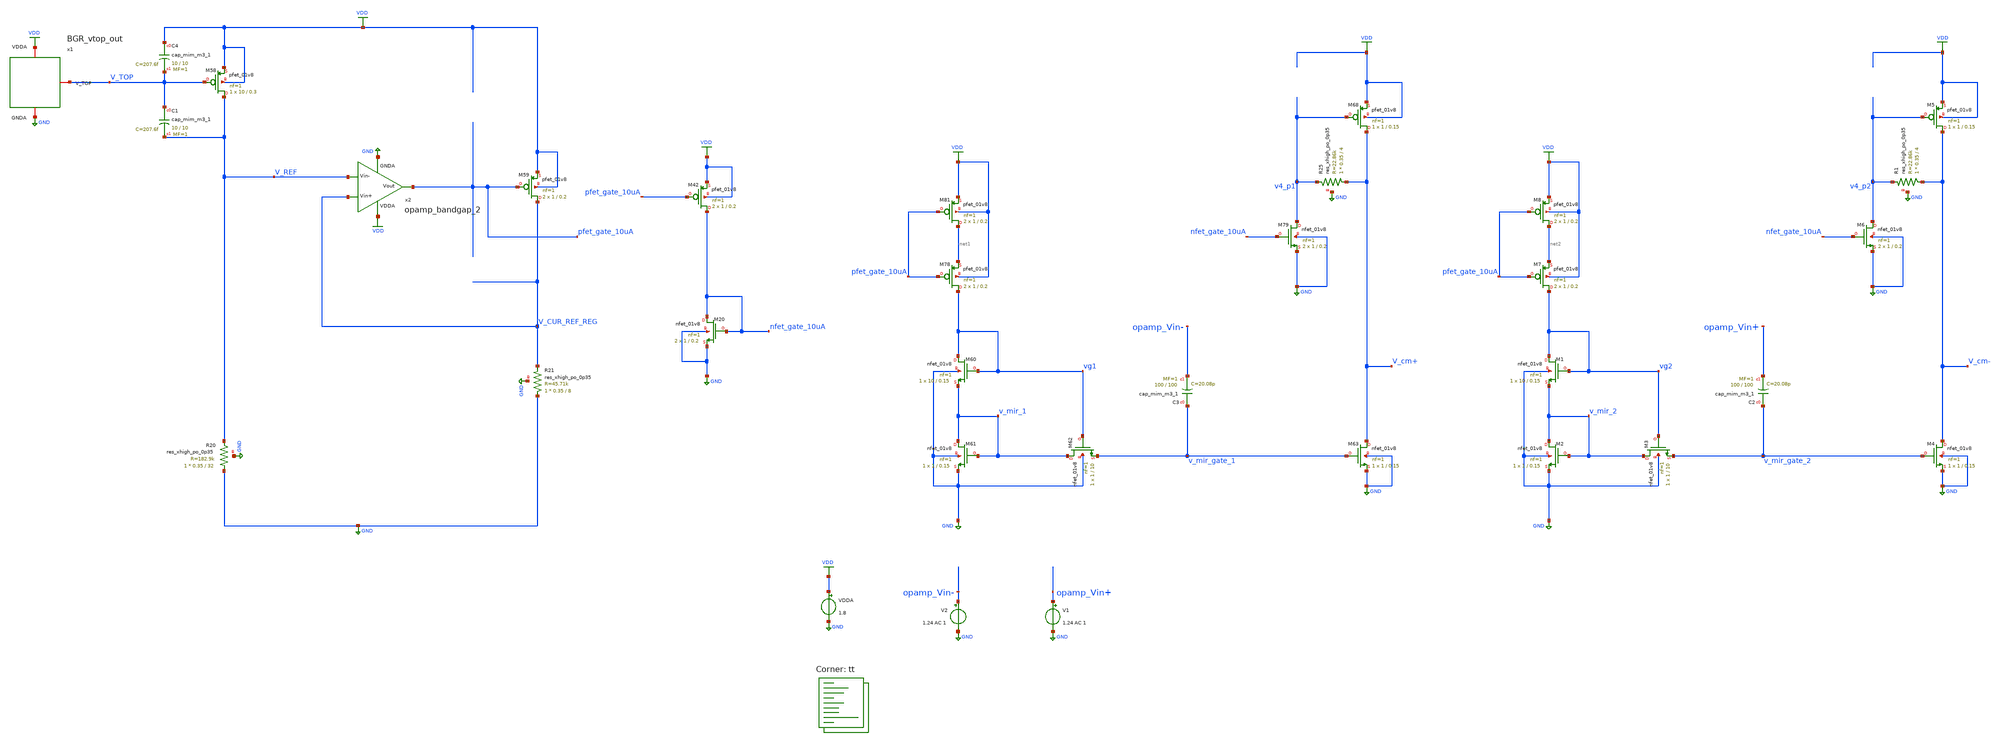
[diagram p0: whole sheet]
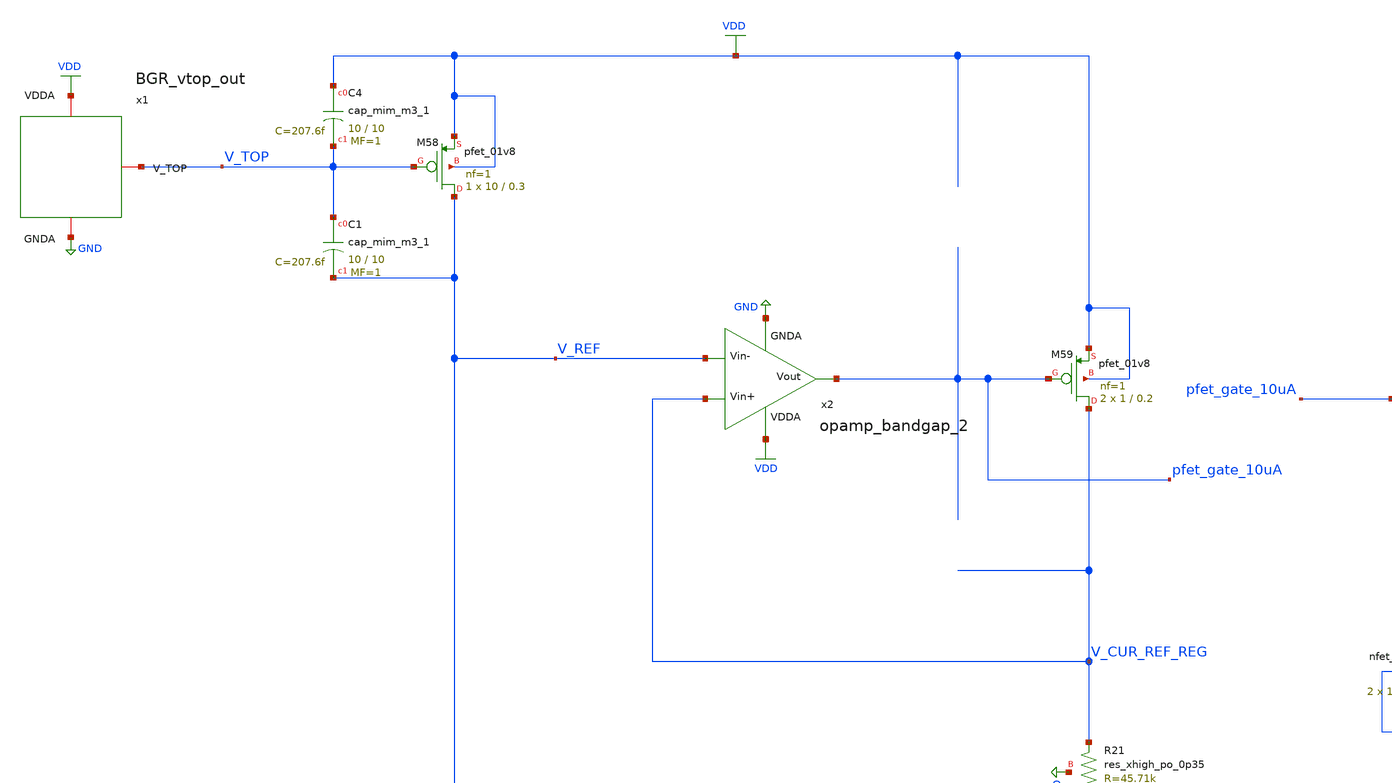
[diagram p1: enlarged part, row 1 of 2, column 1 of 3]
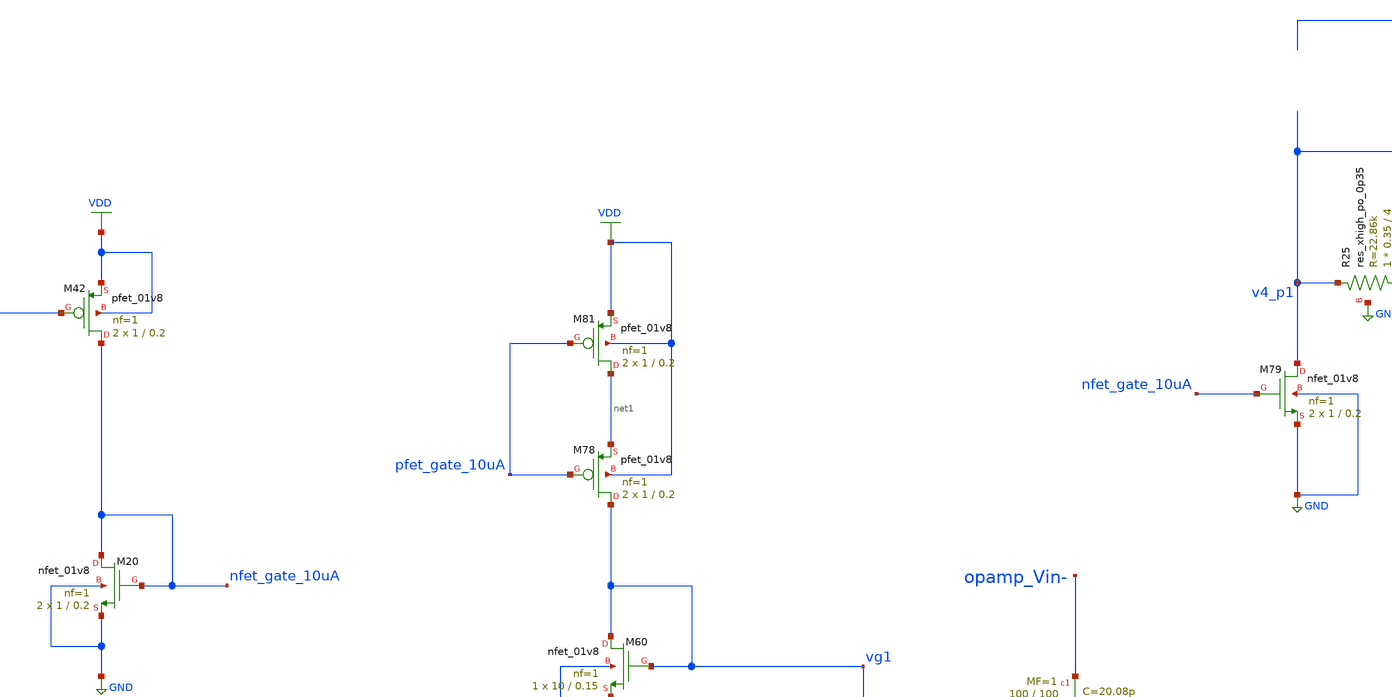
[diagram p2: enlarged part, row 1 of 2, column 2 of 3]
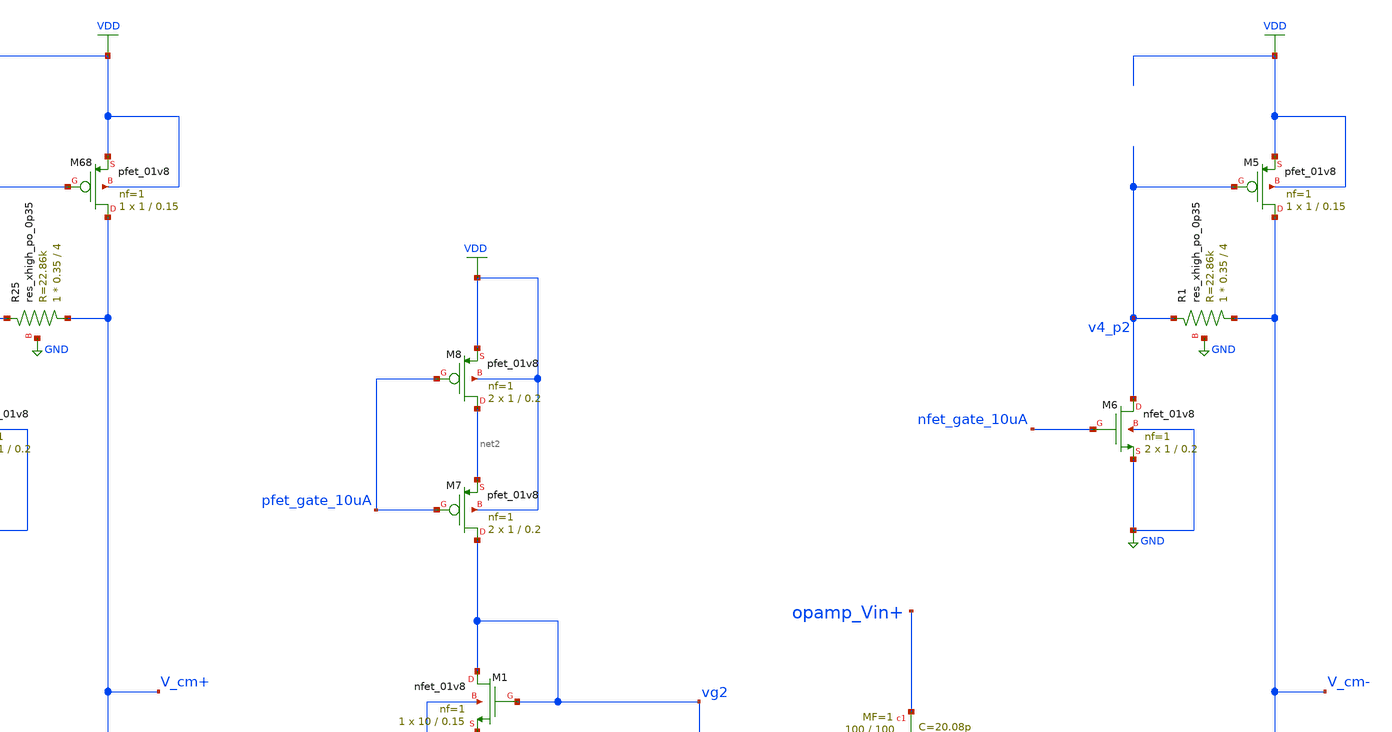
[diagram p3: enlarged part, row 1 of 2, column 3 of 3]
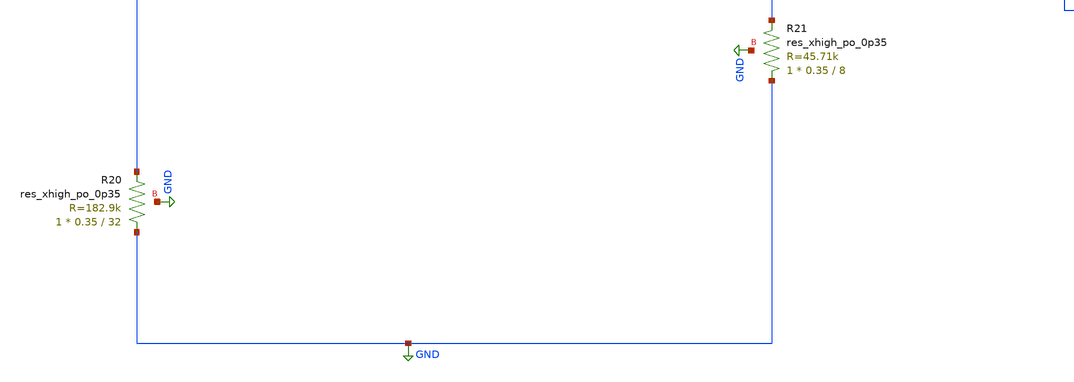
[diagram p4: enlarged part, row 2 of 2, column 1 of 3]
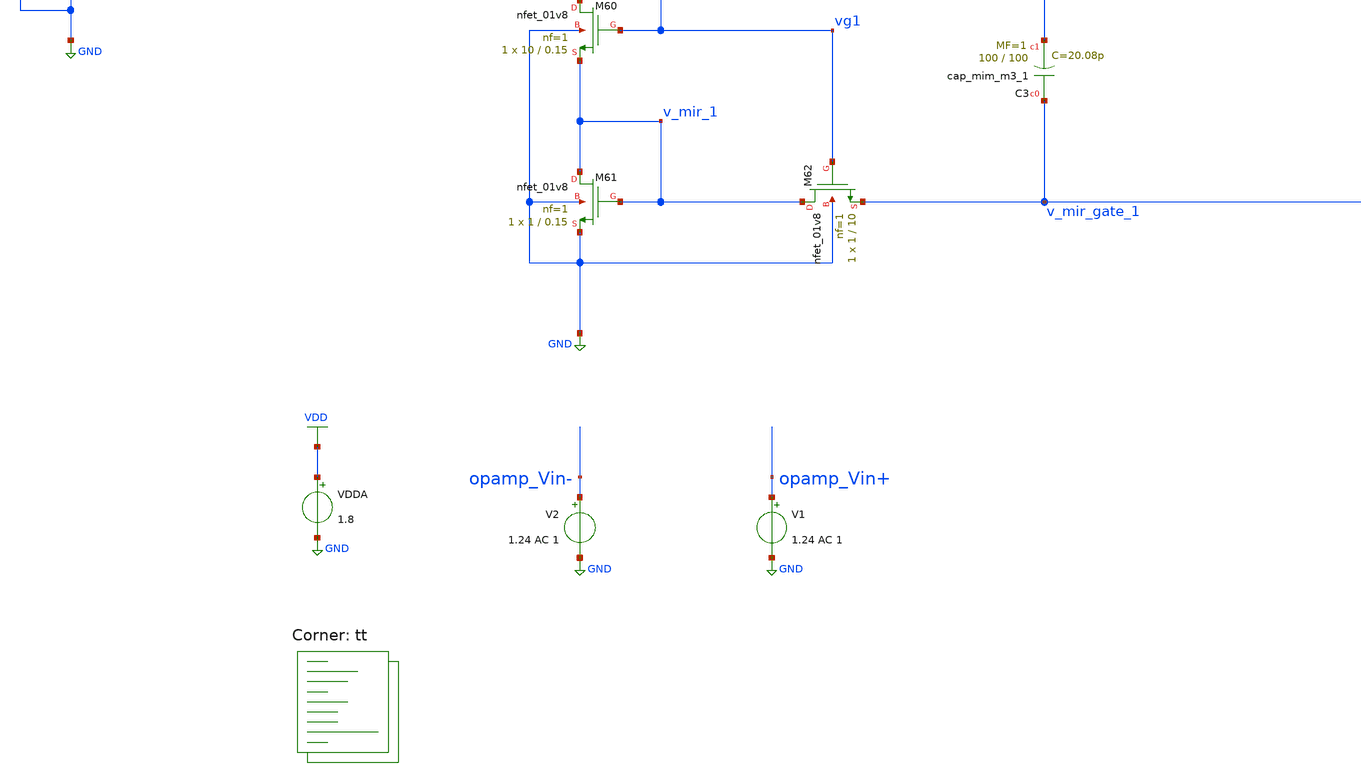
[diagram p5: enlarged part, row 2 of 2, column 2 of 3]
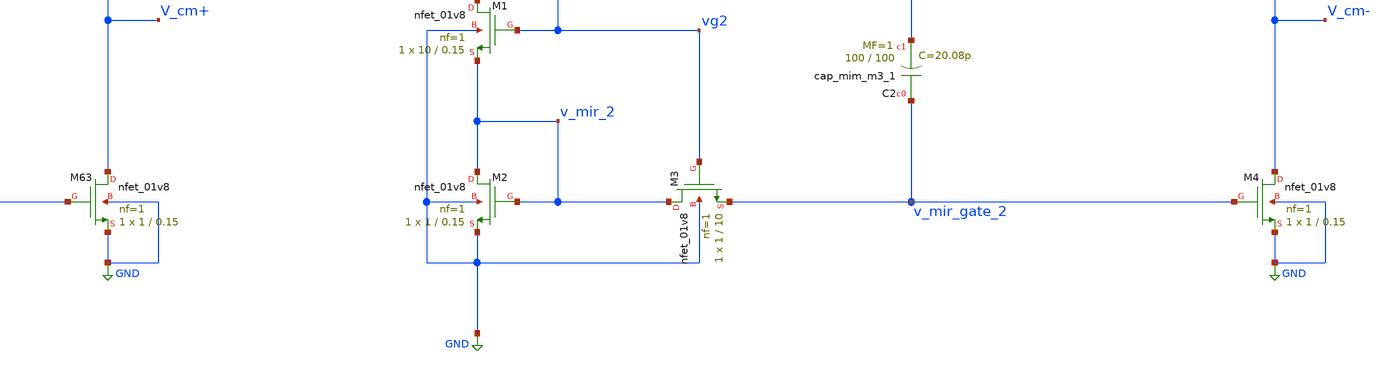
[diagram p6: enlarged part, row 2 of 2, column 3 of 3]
** sch_path: projects/opamp/xschem_ngspice/tb_input_stage.sch
**.subckt tb_input_stage
VDDA VDD GND 1.8
XC3 v_mir_gate_1 opamp_Vin- sky130_fd_pr__cap_mim_m3_1 W=100 L=100 MF=1 m=1
XM60 vg1 vg1 v_mir_1 GND sky130_fd_pr__nfet_01v8 L=0.15 W=10 nf=1 ad='int((nf+1)/2) * W/nf * 0.29' as='int((nf+2)/2) * W/nf * 0.29'
+ pd='2*int((nf+1)/2) * (W/nf + 0.29)' ps='2*int((nf+2)/2) * (W/nf + 0.29)' nrd='0.29 / W' nrs='0.29 / W'
+ sa=0 sb=0 sd=0 mult=1 m=1
XM61 v_mir_1 v_mir_1 GND GND sky130_fd_pr__nfet_01v8 L=0.15 W=1 nf=1 ad='int((nf+1)/2) * W/nf * 0.29'
+ as='int((nf+2)/2) * W/nf * 0.29' pd='2*int((nf+1)/2) * (W/nf + 0.29)' ps='2*int((nf+2)/2) * (W/nf + 0.29)'
+ nrd='0.29 / W' nrs='0.29 / W' sa=0 sb=0 sd=0 mult=1 m=1
XM62 v_mir_1 vg1 v_mir_gate_1 GND sky130_fd_pr__nfet_01v8 L=10 W=1 nf=1 ad='int((nf+1)/2) * W/nf * 0.29'
+ as='int((nf+2)/2) * W/nf * 0.29' pd='2*int((nf+1)/2) * (W/nf + 0.29)' ps='2*int((nf+2)/2) * (W/nf + 0.29)'
+ nrd='0.29 / W' nrs='0.29 / W' sa=0 sb=0 sd=0 mult=1 m=1
XM63 V_cm+ v_mir_gate_1 GND GND sky130_fd_pr__nfet_01v8 L=0.15 W=1 nf=1 ad='int((nf+1)/2) * W/nf * 0.29'
+ as='int((nf+2)/2) * W/nf * 0.29' pd='2*int((nf+1)/2) * (W/nf + 0.29)' ps='2*int((nf+2)/2) * (W/nf + 0.29)'
+ nrd='0.29 / W' nrs='0.29 / W' sa=0 sb=0 sd=0 mult=1 m=1
XM68 V_cm+ v4_p1 VDD VDD sky130_fd_pr__pfet_01v8 L=0.15 W=1 nf=1 ad='int((nf+1)/2) * W/nf * 0.29' as='int((nf+2)/2) * W/nf * 0.29'
+ pd='2*int((nf+1)/2) * (W/nf + 0.29)' ps='2*int((nf+2)/2) * (W/nf + 0.29)' nrd='0.29 / W' nrs='0.29 / W'
+ sa=0 sb=0 sd=0 mult=1 m=1
XR25 V_cm+ v4_p1 GND sky130_fd_pr__res_xhigh_po_0p35 L=4 mult=1 m=1
XM79 v4_p1 nfet_gate_10uA GND GND sky130_fd_pr__nfet_01v8 L=0.2 W=1 nf=1 ad='int((nf+1)/2) * W/nf * 0.29'
+ as='int((nf+2)/2) * W/nf * 0.29' pd='2*int((nf+1)/2) * (W/nf + 0.29)' ps='2*int((nf+2)/2) * (W/nf + 0.29)'
+ nrd='0.29 / W' nrs='0.29 / W' sa=0 sb=0 sd=0 mult=2 m=2
XM78 vg1 pfet_gate_10uA net1 VDD sky130_fd_pr__pfet_01v8 L=0.2 W=1 nf=1 ad='int((nf+1)/2) * W/nf * 0.29'
+ as='int((nf+2)/2) * W/nf * 0.29' pd='2*int((nf+1)/2) * (W/nf + 0.29)' ps='2*int((nf+2)/2) * (W/nf + 0.29)'
+ nrd='0.29 / W' nrs='0.29 / W' sa=0 sb=0 sd=0 mult=2 m=2
XM81 net1 pfet_gate_10uA VDD VDD sky130_fd_pr__pfet_01v8 L=0.2 W=1 nf=1 ad='int((nf+1)/2) * W/nf * 0.29'
+ as='int((nf+2)/2) * W/nf * 0.29' pd='2*int((nf+1)/2) * (W/nf + 0.29)' ps='2*int((nf+2)/2) * (W/nf + 0.29)'
+ nrd='0.29 / W' nrs='0.29 / W' sa=0 sb=0 sd=0 mult=2 m=2
V2 opamp_Vin- GND 1.24 AC 1
V1 opamp_Vin+ GND 1.24 AC 1
XM42 nfet_gate_10uA pfet_gate_10uA VDD VDD sky130_fd_pr__pfet_01v8 L=0.2 W=1 nf=1 ad='int((nf+1)/2) * W/nf * 0.29'
+ as='int((nf+2)/2) * W/nf * 0.29' pd='2*int((nf+1)/2) * (W/nf + 0.29)' ps='2*int((nf+2)/2) * (W/nf + 0.29)'
+ nrd='0.29 / W' nrs='0.29 / W' sa=0 sb=0 sd=0 mult=2 m=2
XM58 V_REF V_TOP VDD VDD sky130_fd_pr__pfet_01v8 L=0.3 W=10 nf=1 ad='int((nf+1)/2) * W/nf * 0.29' as='int((nf+2)/2) * W/nf * 0.29'
+ pd='2*int((nf+1)/2) * (W/nf + 0.29)' ps='2*int((nf+2)/2) * (W/nf + 0.29)' nrd='0.29 / W' nrs='0.29 / W'
+ sa=0 sb=0 sd=0 mult=1 m=1
XR20 GND V_REF GND sky130_fd_pr__res_xhigh_po_0p35 L=32 mult=1 m=1
XR21 GND V_CUR_REF_REG GND sky130_fd_pr__res_xhigh_po_0p35 L=8 mult=1 m=1
XM59 V_CUR_REF_REG pfet_gate_10uA VDD VDD sky130_fd_pr__pfet_01v8 L=0.2 W=1 nf=1 ad='int((nf+1)/2) * W/nf * 0.29'
+ as='int((nf+2)/2) * W/nf * 0.29' pd='2*int((nf+1)/2) * (W/nf + 0.29)' ps='2*int((nf+2)/2) * (W/nf + 0.29)'
+ nrd='0.29 / W' nrs='0.29 / W' sa=0 sb=0 sd=0 mult=2 m=2
x1 V_TOP VDD GND BGR_vtop_out
x2 VDD pfet_gate_10uA V_REF V_CUR_REF_REG GND opamp_bandgap_2
XC1 V_TOP V_REF sky130_fd_pr__cap_mim_m3_1 W=10 L=10 MF=1 m=1
XM20 nfet_gate_10uA nfet_gate_10uA GND GND sky130_fd_pr__nfet_01v8 L=0.2 W=1 nf=1 ad='int((nf+1)/2) * W/nf * 0.29'
+ as='int((nf+2)/2) * W/nf * 0.29' pd='2*int((nf+1)/2) * (W/nf + 0.29)' ps='2*int((nf+2)/2) * (W/nf + 0.29)'
+ nrd='0.29 / W' nrs='0.29 / W' sa=0 sb=0 sd=0 mult=2 m=2
XC4 VDD V_TOP sky130_fd_pr__cap_mim_m3_1 W=10 L=10 MF=1 m=1
XC2 v_mir_gate_2 opamp_Vin+ sky130_fd_pr__cap_mim_m3_1 W=100 L=100 MF=1 m=1
XM1 vg2 vg2 v_mir_2 GND sky130_fd_pr__nfet_01v8 L=0.15 W=10 nf=1 ad='int((nf+1)/2) * W/nf * 0.29' as='int((nf+2)/2) * W/nf * 0.29'
+ pd='2*int((nf+1)/2) * (W/nf + 0.29)' ps='2*int((nf+2)/2) * (W/nf + 0.29)' nrd='0.29 / W' nrs='0.29 / W'
+ sa=0 sb=0 sd=0 mult=1 m=1
XM2 v_mir_2 v_mir_2 GND GND sky130_fd_pr__nfet_01v8 L=0.15 W=1 nf=1 ad='int((nf+1)/2) * W/nf * 0.29'
+ as='int((nf+2)/2) * W/nf * 0.29' pd='2*int((nf+1)/2) * (W/nf + 0.29)' ps='2*int((nf+2)/2) * (W/nf + 0.29)'
+ nrd='0.29 / W' nrs='0.29 / W' sa=0 sb=0 sd=0 mult=1 m=1
XM3 v_mir_2 vg2 v_mir_gate_2 GND sky130_fd_pr__nfet_01v8 L=10 W=1 nf=1 ad='int((nf+1)/2) * W/nf * 0.29'
+ as='int((nf+2)/2) * W/nf * 0.29' pd='2*int((nf+1)/2) * (W/nf + 0.29)' ps='2*int((nf+2)/2) * (W/nf + 0.29)'
+ nrd='0.29 / W' nrs='0.29 / W' sa=0 sb=0 sd=0 mult=1 m=1
XM4 V_cm- v_mir_gate_2 GND GND sky130_fd_pr__nfet_01v8 L=0.15 W=1 nf=1 ad='int((nf+1)/2) * W/nf * 0.29'
+ as='int((nf+2)/2) * W/nf * 0.29' pd='2*int((nf+1)/2) * (W/nf + 0.29)' ps='2*int((nf+2)/2) * (W/nf + 0.29)'
+ nrd='0.29 / W' nrs='0.29 / W' sa=0 sb=0 sd=0 mult=1 m=1
XM5 V_cm- v4_p2 VDD VDD sky130_fd_pr__pfet_01v8 L=0.15 W=1 nf=1 ad='int((nf+1)/2) * W/nf * 0.29' as='int((nf+2)/2) * W/nf * 0.29'
+ pd='2*int((nf+1)/2) * (W/nf + 0.29)' ps='2*int((nf+2)/2) * (W/nf + 0.29)' nrd='0.29 / W' nrs='0.29 / W'
+ sa=0 sb=0 sd=0 mult=1 m=1
XR1 V_cm- v4_p2 GND sky130_fd_pr__res_xhigh_po_0p35 L=4 mult=1 m=1
XM6 v4_p2 nfet_gate_10uA GND GND sky130_fd_pr__nfet_01v8 L=0.2 W=1 nf=1 ad='int((nf+1)/2) * W/nf * 0.29'
+ as='int((nf+2)/2) * W/nf * 0.29' pd='2*int((nf+1)/2) * (W/nf + 0.29)' ps='2*int((nf+2)/2) * (W/nf + 0.29)'
+ nrd='0.29 / W' nrs='0.29 / W' sa=0 sb=0 sd=0 mult=2 m=2
XM7 vg2 pfet_gate_10uA net2 VDD sky130_fd_pr__pfet_01v8 L=0.2 W=1 nf=1 ad='int((nf+1)/2) * W/nf * 0.29'
+ as='int((nf+2)/2) * W/nf * 0.29' pd='2*int((nf+1)/2) * (W/nf + 0.29)' ps='2*int((nf+2)/2) * (W/nf + 0.29)'
+ nrd='0.29 / W' nrs='0.29 / W' sa=0 sb=0 sd=0 mult=2 m=2
XM8 net2 pfet_gate_10uA VDD VDD sky130_fd_pr__pfet_01v8 L=0.2 W=1 nf=1 ad='int((nf+1)/2) * W/nf * 0.29'
+ as='int((nf+2)/2) * W/nf * 0.29' pd='2*int((nf+1)/2) * (W/nf + 0.29)' ps='2*int((nf+2)/2) * (W/nf + 0.29)'
+ nrd='0.29 / W' nrs='0.29 / W' sa=0 sb=0 sd=0 mult=2 m=2
**** begin user architecture code
.lib $::SKYWATER_MODELS/sky130.lib.spice tt




.option wnflag=1
.option savecurrents

* .param VDDGAUSS = agauss(1.8, 0.05, 1)
* .param VDD = VDDGAUSS
* .param VDD = 1.8

* .param TEMPGAUSS = agauss(40, 30, 1)
* .param temp = TEMPGAUSS
* .option temp = 26

.save @m.xm1.msky130_fd_pr__pfet_01v8[gm] @m.xm1.msky130_fd_pr__pfet_01v8[vds] @m.xm1.msky130_fd_pr__pfet_01v8[vth] @m.xm2.msky130_fd_pr__pfet_01v8[gm] @m.xm2.msky130_fd_pr__pfet_01v8[vds] @m.xm2.msky130_fd_pr__pfet_01v8[vth] @m.xm3.msky130_fd_pr__nfet_01v8[gm] @m.xm3.msky130_fd_pr__nfet_01v8[vds] @m.xm3.msky130_fd_pr__nfet_01v8[vth] @m.xm4.msky130_fd_pr__nfet_01v8[gm] @m.xm4.msky130_fd_pr__nfet_01v8[vds] @m.xm4.msky130_fd_pr__nfet_01v8[vth] @m.xm5.msky130_fd_pr__pfet_01v8[gm] @m.xm5.msky130_fd_pr__pfet_01v8[vds] @m.xm5.msky130_fd_pr__pfet_01v8[vth] @m.xm6.msky130_fd_pr__pfet_01v8[gm] @m.xm6.msky130_fd_pr__pfet_01v8[vds] @m.xm6.msky130_fd_pr__pfet_01v8[vth] @m.xm7.msky130_fd_pr__pfet_01v8[gm] @m.xm7.msky130_fd_pr__pfet_01v8[vds] @m.xm7.msky130_fd_pr__pfet_01v8[vth] @m.xm8.msky130_fd_pr__pfet_01v8[gm] @m.xm8.msky130_fd_pr__pfet_01v8[vds] @m.xm8.msky130_fd_pr__pfet_01v8[vth]

.control

  save all

  * tran 1000p 2000n
  * tran 100p 2u
  * tran 20n 0.2m
  ac dec 20 1 1T
  write tb_input_stage.raw
  set appendwrite
  show

.endc




**** end user architecture code
**.ends

* expanding   symbol:
*+  /foss/designs/my_design/projects/bandgapref/xschem_ngspice/new_files/BGR_vtop_out.sym # of pins=3
** sym_path: projects/bandgapref/xschem_ngspice/new_files/BGR_vtop_out.sym
** sch_path: projects/bandgapref/xschem_ngspice/new_files/BGR_vtop_out.sch
.subckt BGR_vtop_out V_TOP VDDA GNDA
*.iopin VDDA
*.iopin GNDA
*.opin V_TOP
XQ1 GNDA GNDA Vin- sky130_fd_pr__pnp_05v5_W3p40L3p40 m=1
XQ2 GNDA GNDA Vbe2 sky130_fd_pr__pnp_05v5_W3p40L3p40 m=8
XM1 Vin- V_TOP VDDA VDDA sky130_fd_pr__pfet_01v8 L=0.5 W=10 nf=1 ad='int((nf+1)/2) * W/nf * 0.29' as='int((nf+2)/2) * W/nf * 0.29'
+ pd='2*int((nf+1)/2) * (W/nf + 0.29)' ps='2*int((nf+2)/2) * (W/nf + 0.29)' nrd='0.29 / W' nrs='0.29 / W'
+ sa=0 sb=0 sd=0 mult=1 m=1
XM2 Vin+ V_TOP VDDA VDDA sky130_fd_pr__pfet_01v8 L=0.5 W=10 nf=1 ad='int((nf+1)/2) * W/nf * 0.29' as='int((nf+2)/2) * W/nf * 0.29'
+ pd='2*int((nf+1)/2) * (W/nf + 0.29)' ps='2*int((nf+2)/2) * (W/nf + 0.29)' nrd='0.29 / W' nrs='0.29 / W'
+ sa=0 sb=0 sd=0 mult=1 m=1
XR1 Vbe2 Vin+ GNDA sky130_fd_pr__res_xhigh_po_0p35 L=2.3 mult=1 m=1
XR2 GNDA Vin+ GNDA sky130_fd_pr__res_xhigh_po_0p35 L=18 mult=1 m=1
XR3 GNDA Vin- GNDA sky130_fd_pr__res_xhigh_po_0p35 L=18 mult=1 m=1
XM5 start_up start_up start_up_nfet1 start_up_nfet1 sky130_fd_pr__nfet_01v8 L=10 W=1 nf=1 ad='int((nf+1)/2) * W/nf * 0.29'
+ as='int((nf+2)/2) * W/nf * 0.29' pd='2*int((nf+1)/2) * (W/nf + 0.29)' ps='2*int((nf+2)/2) * (W/nf + 0.29)'
+ nrd='0.29 / W' nrs='0.29 / W' sa=0 sb=0 sd=0 mult=1 m=1
XM6 start_up V_TOP VDDA VDDA sky130_fd_pr__pfet_01v8 L=0.5 W=10 nf=1 ad='int((nf+1)/2) * W/nf * 0.29'
+ as='int((nf+2)/2) * W/nf * 0.29' pd='2*int((nf+1)/2) * (W/nf + 0.29)' ps='2*int((nf+2)/2) * (W/nf + 0.29)'
+ nrd='0.29 / W' nrs='0.29 / W' sa=0 sb=0 sd=0 mult=1 m=1
XM4 Vin- start_up V_TOP VDDA sky130_fd_pr__pfet_01v8 L=0.15 W=2 nf=1 ad='int((nf+1)/2) * W/nf * 0.29'
+ as='int((nf+2)/2) * W/nf * 0.29' pd='2*int((nf+1)/2) * (W/nf + 0.29)' ps='2*int((nf+2)/2) * (W/nf + 0.29)'
+ nrd='0.29 / W' nrs='0.29 / W' sa=0 sb=0 sd=0 mult=1 m=1
XM7 start_up_nfet1 start_up_nfet1 GNDA GNDA sky130_fd_pr__nfet_01v8 L=10 W=1 nf=1 ad='int((nf+1)/2) * W/nf * 0.29'
+ as='int((nf+2)/2) * W/nf * 0.29' pd='2*int((nf+1)/2) * (W/nf + 0.29)' ps='2*int((nf+2)/2) * (W/nf + 0.29)'
+ nrd='0.29 / W' nrs='0.29 / W' sa=0 sb=0 sd=0 mult=1 m=1
x1 VDDA V_TOP Vin- Vin+ GNDA opamp_bandgap_2
.ends


* expanding   symbol:
*+  /foss/designs/my_design/projects/bandgapref/xschem_ngspice/new_files/opamp_bandgap_2.sym # of pins=5
** sym_path: projects/bandgapref/xschem_ngspice/new_files/opamp_bandgap_2.sym
** sch_path: projects/bandgapref/xschem_ngspice/new_files/opamp_bandgap_2.sch
.subckt opamp_bandgap_2 VDDA Vout Vin- Vin+ GNDA
*.ipin Vin+
*.opin Vout
*.ipin Vin-
*.ipin GNDA
*.ipin VDDA
XM1 V_p VDDA GNDA GNDA sky130_fd_pr__nfet_01v8 L=5 W=2.5 nf=1 ad='int((nf+1)/2) * W/nf * 0.29' as='int((nf+2)/2) * W/nf * 0.29'
+ pd='2*int((nf+1)/2) * (W/nf + 0.29)' ps='2*int((nf+2)/2) * (W/nf + 0.29)' nrd='0.29 / W' nrs='0.29 / W'
+ sa=0 sb=0 sd=0 mult=1 m=1
XM2 V_mirror Vin- V_p GNDA sky130_fd_pr__nfet_01v8 L=0.2 W=2.5 nf=1 ad='int((nf+1)/2) * W/nf * 0.29'
+ as='int((nf+2)/2) * W/nf * 0.29' pd='2*int((nf+1)/2) * (W/nf + 0.29)' ps='2*int((nf+2)/2) * (W/nf + 0.29)'
+ nrd='0.29 / W' nrs='0.29 / W' sa=0 sb=0 sd=0 mult=1 m=1
XM3 1st_Vout Vin+ V_p GNDA sky130_fd_pr__nfet_01v8 L=0.2 W=2.5 nf=1 ad='int((nf+1)/2) * W/nf * 0.29'
+ as='int((nf+2)/2) * W/nf * 0.29' pd='2*int((nf+1)/2) * (W/nf + 0.29)' ps='2*int((nf+2)/2) * (W/nf + 0.29)'
+ nrd='0.29 / W' nrs='0.29 / W' sa=0 sb=0 sd=0 mult=1 m=1
XM5 V_mirror V_mirror VDDA VDDA sky130_fd_pr__pfet_01v8 L=0.2 W=6 nf=2 ad='int((nf+1)/2) * W/nf * 0.29'
+ as='int((nf+2)/2) * W/nf * 0.29' pd='2*int((nf+1)/2) * (W/nf + 0.29)' ps='2*int((nf+2)/2) * (W/nf + 0.29)'
+ nrd='0.29 / W' nrs='0.29 / W' sa=0 sb=0 sd=0 mult=1 m=1
XM6 1st_Vout V_mirror VDDA VDDA sky130_fd_pr__pfet_01v8 L=0.2 W=6 nf=2 ad='int((nf+1)/2) * W/nf * 0.29'
+ as='int((nf+2)/2) * W/nf * 0.29' pd='2*int((nf+1)/2) * (W/nf + 0.29)' ps='2*int((nf+2)/2) * (W/nf + 0.29)'
+ nrd='0.29 / W' nrs='0.29 / W' sa=0 sb=0 sd=0 mult=1 m=1
XM4 Vout VDDA GNDA GNDA sky130_fd_pr__nfet_01v8 L=5 W=2.5 nf=1 ad='int((nf+1)/2) * W/nf * 0.29' as='int((nf+2)/2) * W/nf * 0.29'
+ pd='2*int((nf+1)/2) * (W/nf + 0.29)' ps='2*int((nf+2)/2) * (W/nf + 0.29)' nrd='0.29 / W' nrs='0.29 / W'
+ sa=0 sb=0 sd=0 mult=1 m=1
XM7 Vout 1st_Vout VDDA VDDA sky130_fd_pr__pfet_01v8 L=0.2 W=6 nf=2 ad='int((nf+1)/2) * W/nf * 0.29' as='int((nf+2)/2) * W/nf * 0.29'
+ pd='2*int((nf+1)/2) * (W/nf + 0.29)' ps='2*int((nf+2)/2) * (W/nf + 0.29)' nrd='0.29 / W' nrs='0.29 / W'
+ sa=0 sb=0 sd=0 mult=1 m=1
XC1 1st_Vout net1 sky130_fd_pr__cap_mim_m3_1 W=10 L=10 MF=1 m=1
XR1 Vout net1 GNDA sky130_fd_pr__res_xhigh_po_0p35 L=0.5 mult=1 m=1
.ends

.GLOBAL GND
.GLOBAL VDD
.end
